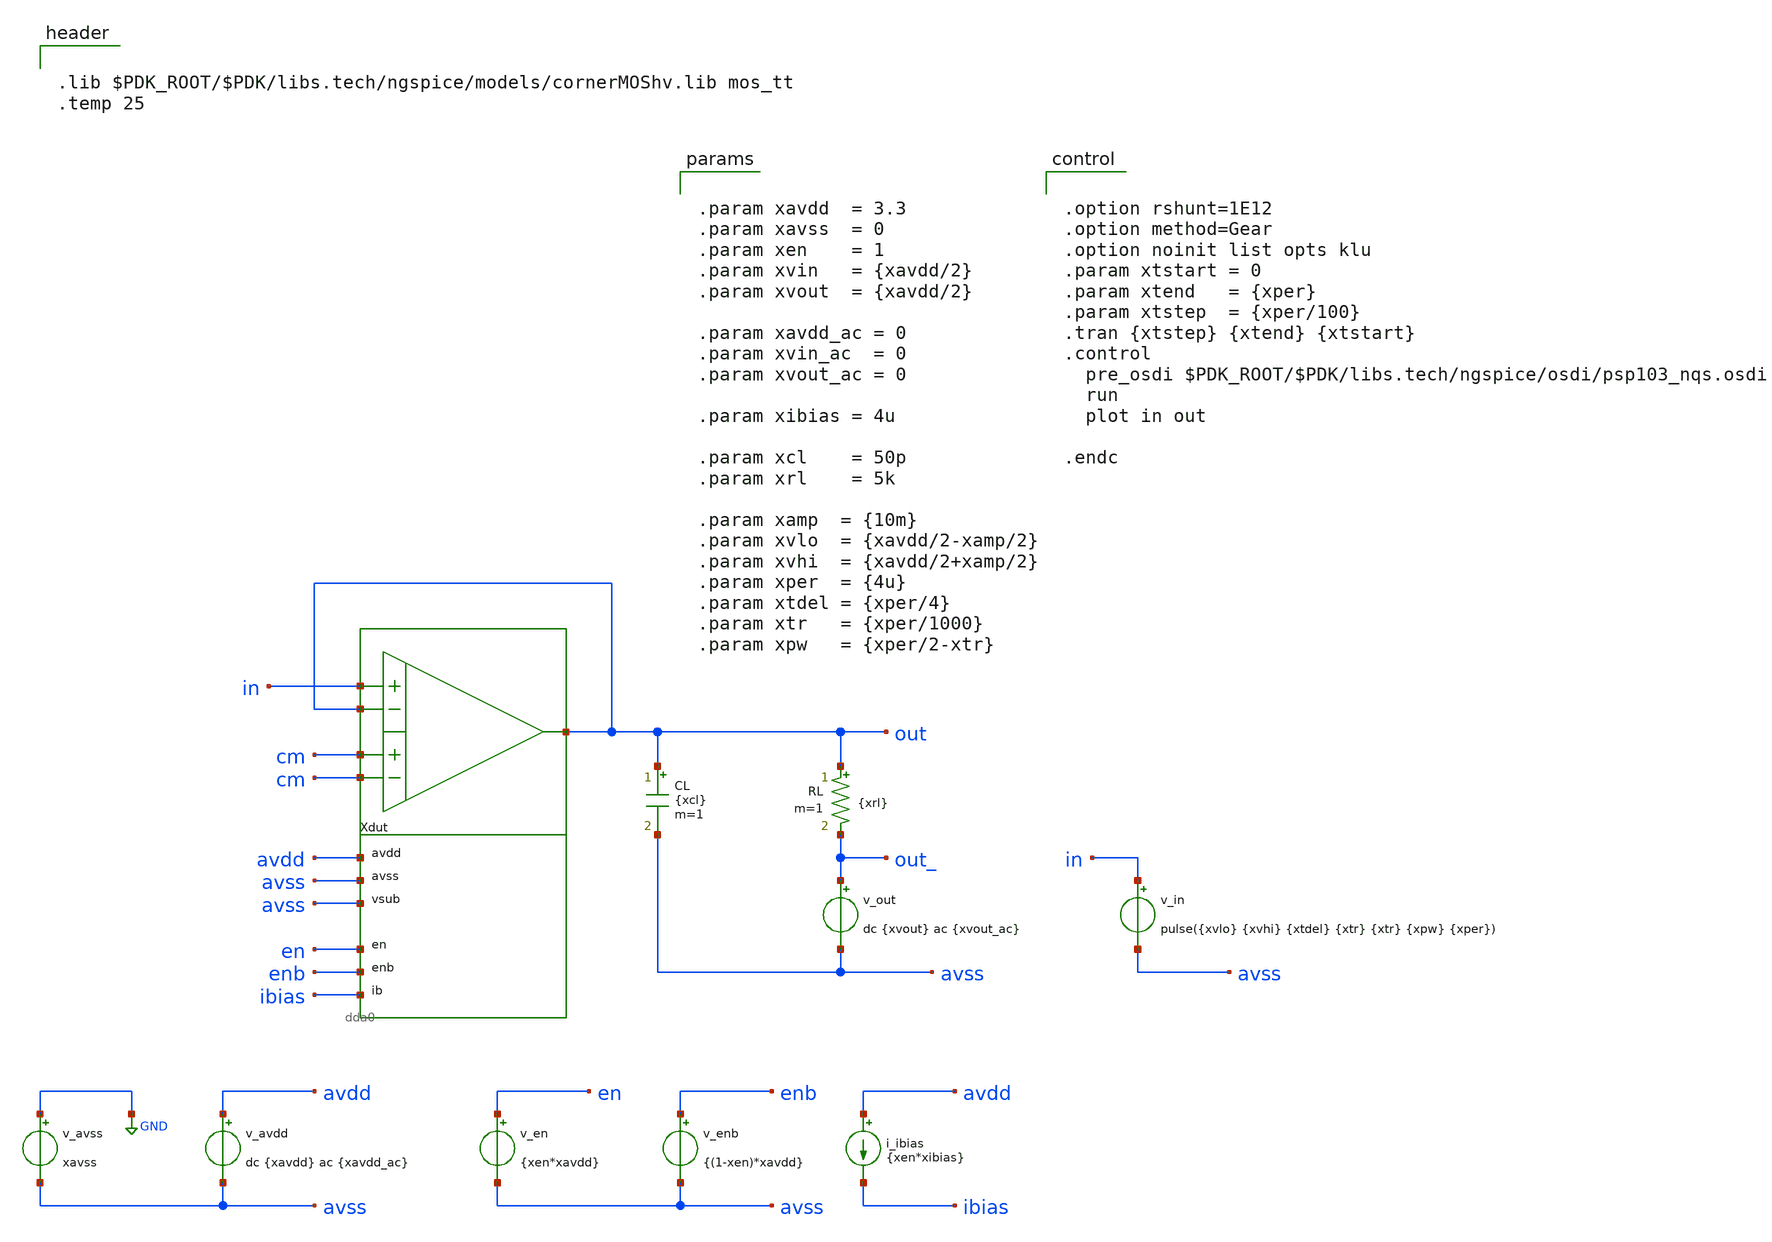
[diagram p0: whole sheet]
** sch_path: xschem/tb_dda0_buf_tran_step_small.sch
**.subckt tb_dda0_buf_tran_step_small
Xdut in out cm cm out avdd avss avss en enb ibias dda0
v_avss GND avss xavss
v_avdd avdd avss dc {xavdd} ac {xavdd_ac}
v_in in avss pulse({xvlo} {xvhi} {xtdel} {xtr} {xtr} {xpw} {xper})
v_en en avss {xen*xavdd}
v_enb enb avss {(1-xen)*xavdd}
i_ibias avdd ibias {xen*xibias}
CL out avss {xcl} m=1
v_out out_ avss dc {xvout} ac {xvout_ac}
RL out out_ {xrl} m=1
**** begin user architecture code


.lib $PDK_ROOT/$PDK/libs.tech/ngspice/models/cornerMOShv.lib mos_tt
.temp 25




.option rshunt=1E12
.option method=Gear
.option noinit list opts klu
.param xtstart = 0
.param xtend   = {xper}
.param xtstep  = {xper/100}
.tran {xtstep} {xtend} {xtstart}
.control
  pre_osdi $PDK_ROOT/$PDK/libs.tech/ngspice/osdi/psp103_nqs.osdi
  run
  plot in out

.endc




.param xavdd  = 3.3
.param xavss  = 0
.param xen    = 1
.param xvin   = {xavdd/2}
.param xvout  = {xavdd/2}

.param xavdd_ac = 0
.param xvin_ac  = 0
.param xvout_ac = 0

.param xibias = 4u

.param xcl    = 50p
.param xrl    = 5k

.param xamp  = {10m}
.param xvlo  = {xavdd/2-xamp/2}
.param xvhi  = {xavdd/2+xamp/2}
.param xper  = {4u}
.param xtdel = {xper/4}
.param xtr   = {xper/1000}
.param xpw   = {xper/2-xtr}


**** end user architecture code
**.ends
.GLOBAL GND
.end
